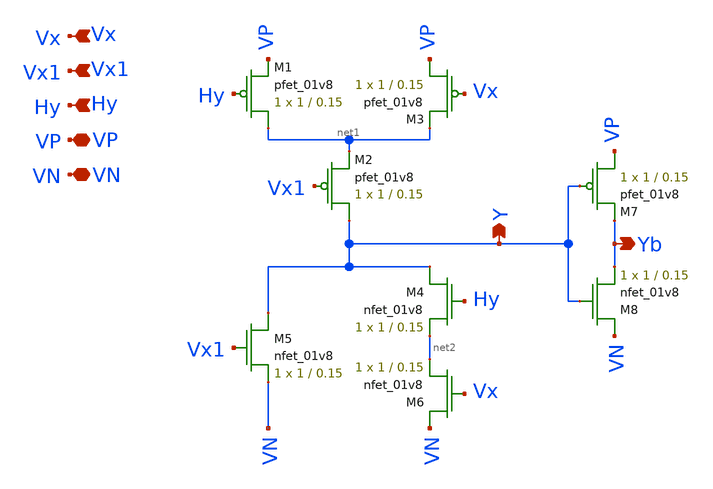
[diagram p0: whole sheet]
** sch_path: mp5/xschem/unit_cell_decoder.sch
**.subckt unit_cell_decoder Vx Vx1 Hy VP VN Y Yb
*.ipin Vx
*.ipin Vx1
*.ipin Hy
*.iopin VP
*.iopin VN
*.opin Y
*.opin Yb
XM1 net1 Hy VP VDD sky130_fd_pr__pfet_01v8 L=0.15 W=1 nf=1 ad='int((nf+1)/2) * W/nf * 0.29' as='int((nf+2)/2) * W/nf * 0.29'
+ pd='2*int((nf+1)/2) * (W/nf + 0.29)' ps='2*int((nf+2)/2) * (W/nf + 0.29)' nrd='0.29 / W' nrs='0.29 / W'
+ sa=0 sb=0 sd=0 mult=1 m=1
XM2 Y Vx1 net1 VDD sky130_fd_pr__pfet_01v8 L=0.15 W=1 nf=1 ad='int((nf+1)/2) * W/nf * 0.29' as='int((nf+2)/2) * W/nf * 0.29'
+ pd='2*int((nf+1)/2) * (W/nf + 0.29)' ps='2*int((nf+2)/2) * (W/nf + 0.29)' nrd='0.29 / W' nrs='0.29 / W'
+ sa=0 sb=0 sd=0 mult=1 m=1
XM3 VP Vx net1 VDD sky130_fd_pr__pfet_01v8 L=0.15 W=1 nf=1 ad='int((nf+1)/2) * W/nf * 0.29' as='int((nf+2)/2) * W/nf * 0.29'
+ pd='2*int((nf+1)/2) * (W/nf + 0.29)' ps='2*int((nf+2)/2) * (W/nf + 0.29)' nrd='0.29 / W' nrs='0.29 / W'
+ sa=0 sb=0 sd=0 mult=1 m=1
XM4 Y Hy net2 GND sky130_fd_pr__nfet_01v8 L=0.15 W=1 nf=1 ad='int((nf+1)/2) * W/nf * 0.29' as='int((nf+2)/2) * W/nf * 0.29'
+ pd='2*int((nf+1)/2) * (W/nf + 0.29)' ps='2*int((nf+2)/2) * (W/nf + 0.29)' nrd='0.29 / W' nrs='0.29 / W'
+ sa=0 sb=0 sd=0 mult=1 m=1
XM5 Y Vx1 VN GND sky130_fd_pr__nfet_01v8 L=0.15 W=1 nf=1 ad='int((nf+1)/2) * W/nf * 0.29' as='int((nf+2)/2) * W/nf * 0.29'
+ pd='2*int((nf+1)/2) * (W/nf + 0.29)' ps='2*int((nf+2)/2) * (W/nf + 0.29)' nrd='0.29 / W' nrs='0.29 / W'
+ sa=0 sb=0 sd=0 mult=1 m=1
XM6 VN Vx net2 GND sky130_fd_pr__nfet_01v8 L=0.15 W=1 nf=1 ad='int((nf+1)/2) * W/nf * 0.29' as='int((nf+2)/2) * W/nf * 0.29'
+ pd='2*int((nf+1)/2) * (W/nf + 0.29)' ps='2*int((nf+2)/2) * (W/nf + 0.29)' nrd='0.29 / W' nrs='0.29 / W'
+ sa=0 sb=0 sd=0 mult=1 m=1
XM7 VP Y Yb VDD sky130_fd_pr__pfet_01v8 L=0.15 W=1 nf=1 ad='int((nf+1)/2) * W/nf * 0.29' as='int((nf+2)/2) * W/nf * 0.29'
+ pd='2*int((nf+1)/2) * (W/nf + 0.29)' ps='2*int((nf+2)/2) * (W/nf + 0.29)' nrd='0.29 / W' nrs='0.29 / W'
+ sa=0 sb=0 sd=0 mult=1 m=1
XM8 VN Y Yb GND sky130_fd_pr__nfet_01v8 L=0.15 W=1 nf=1 ad='int((nf+1)/2) * W/nf * 0.29' as='int((nf+2)/2) * W/nf * 0.29'
+ pd='2*int((nf+1)/2) * (W/nf + 0.29)' ps='2*int((nf+2)/2) * (W/nf + 0.29)' nrd='0.29 / W' nrs='0.29 / W'
+ sa=0 sb=0 sd=0 mult=1 m=1
**.ends
.end
